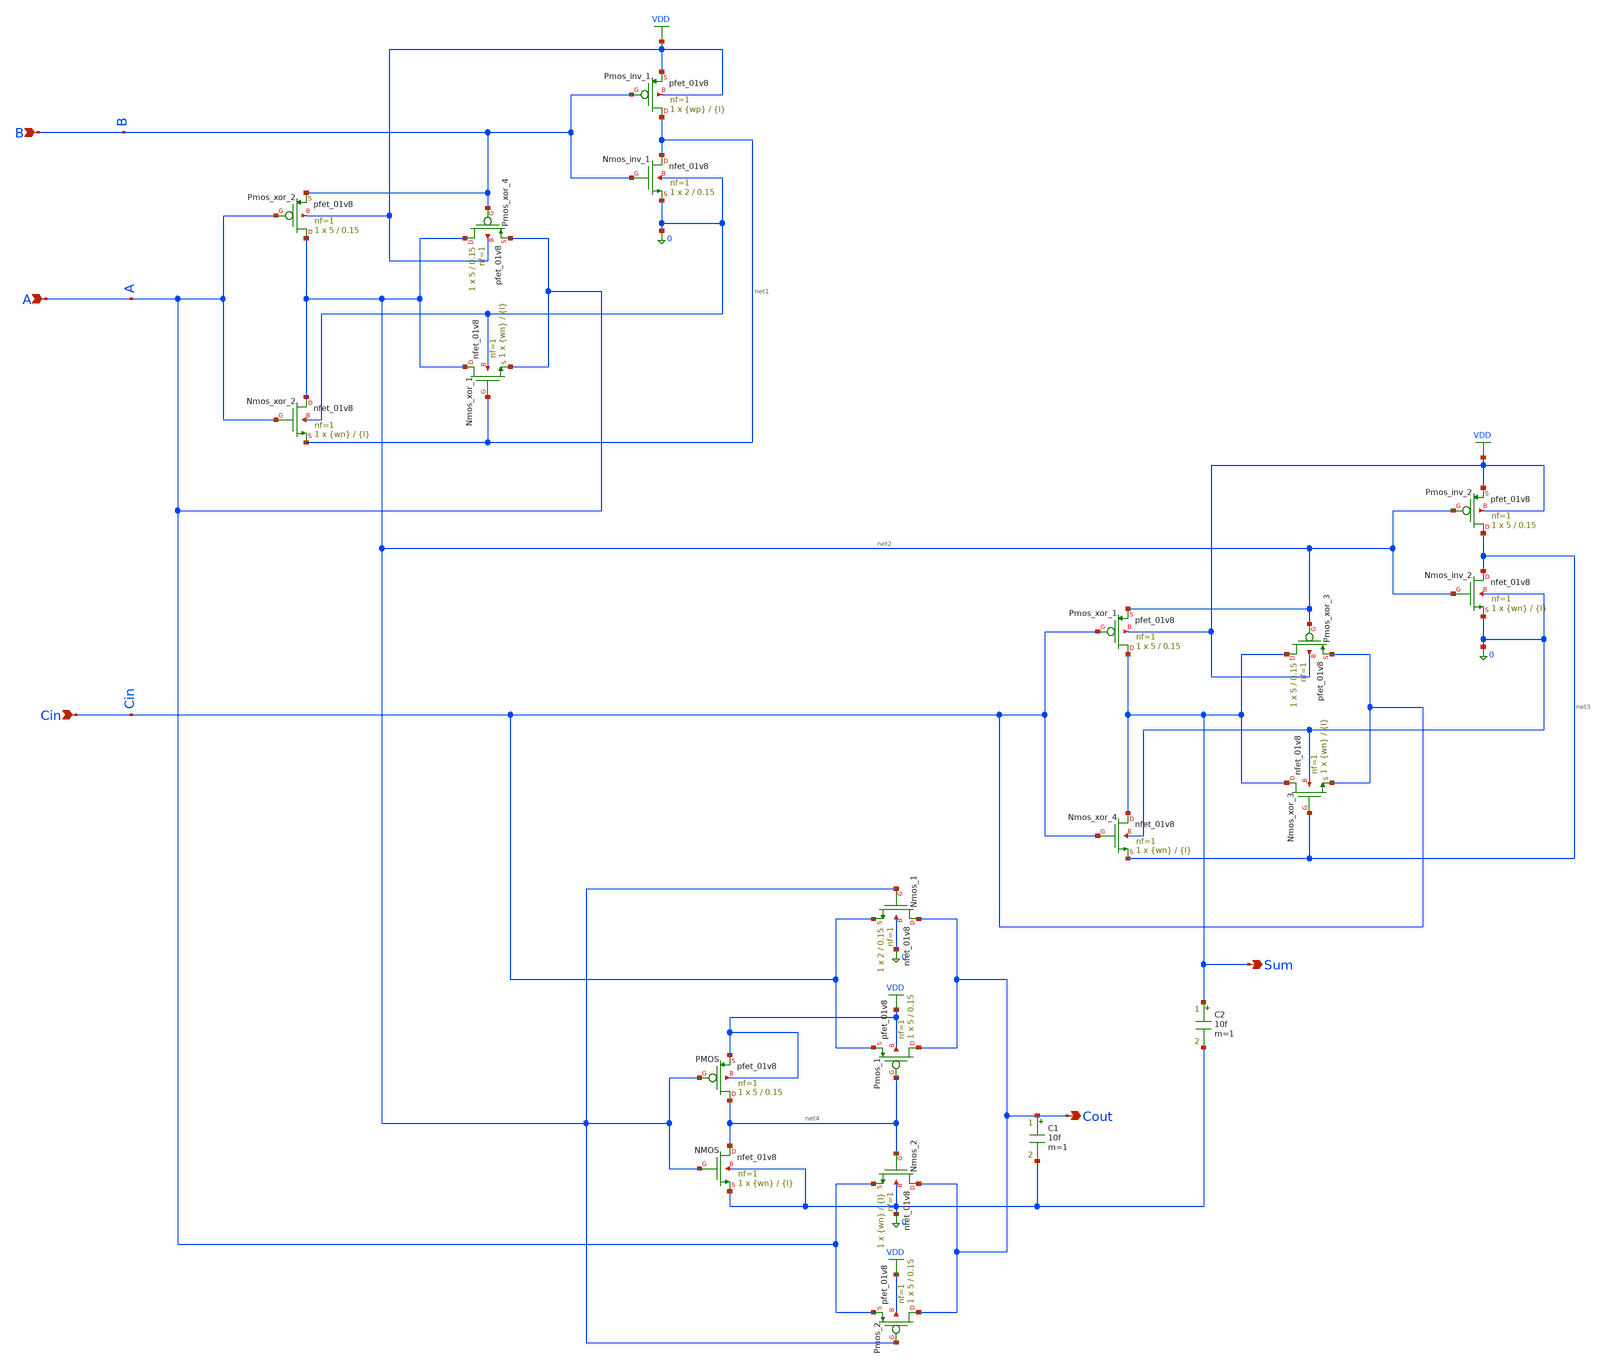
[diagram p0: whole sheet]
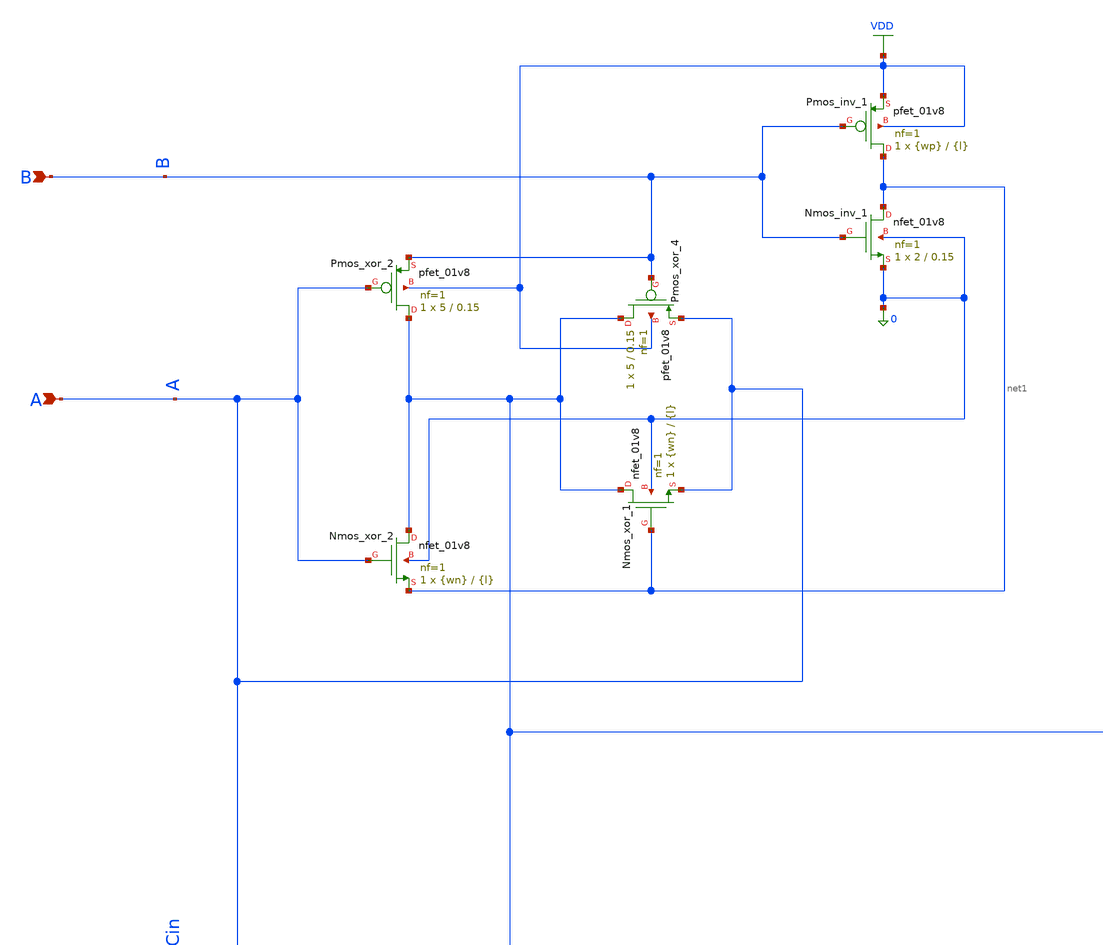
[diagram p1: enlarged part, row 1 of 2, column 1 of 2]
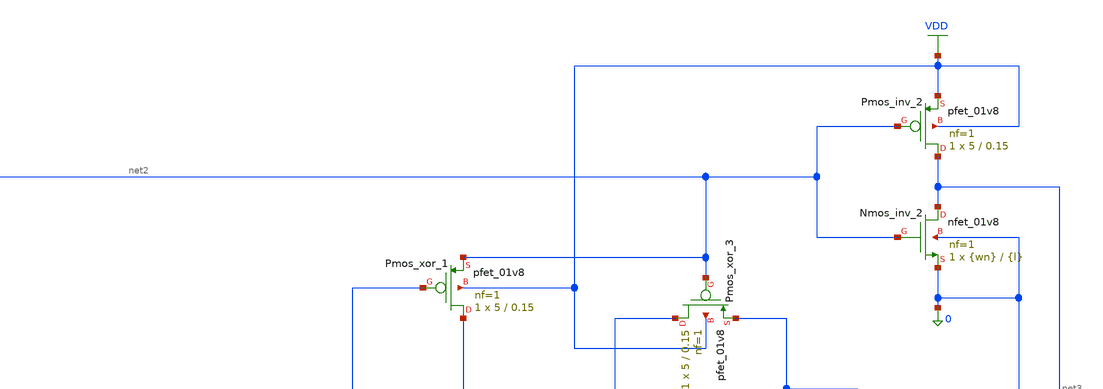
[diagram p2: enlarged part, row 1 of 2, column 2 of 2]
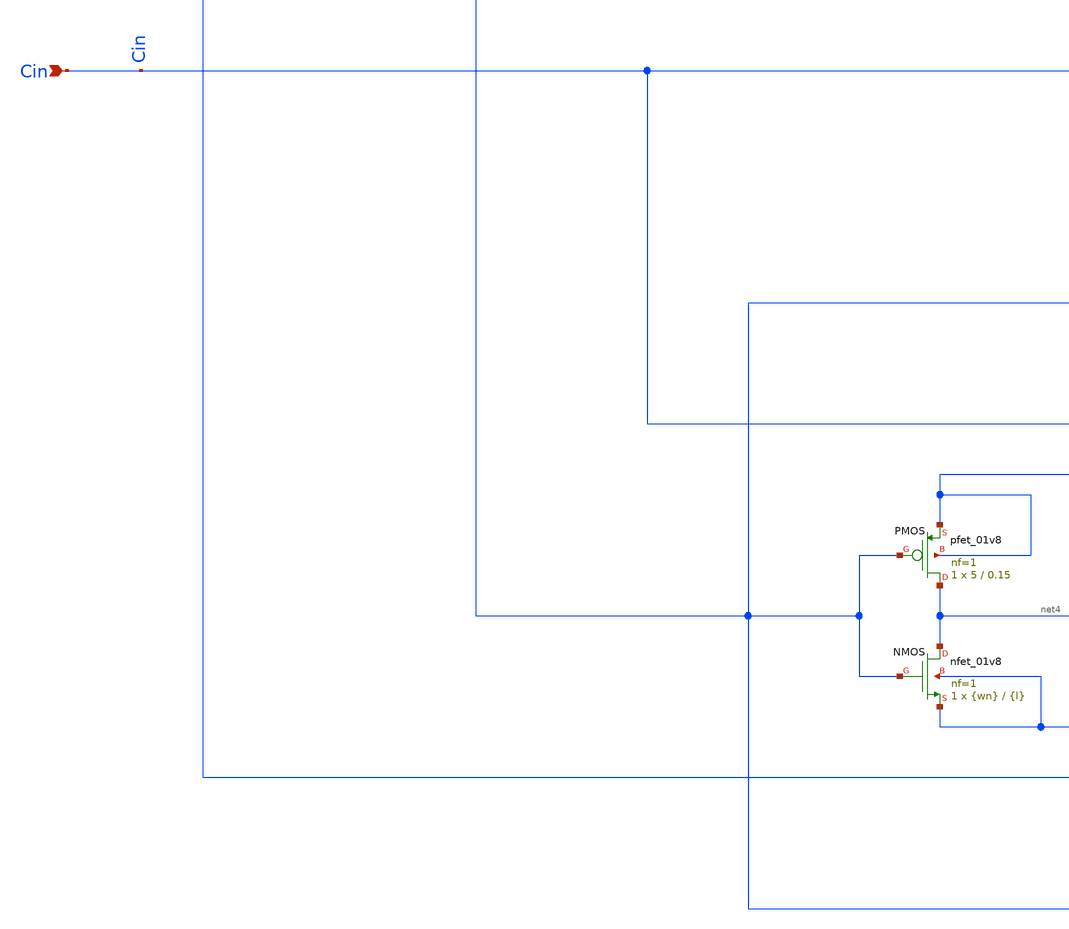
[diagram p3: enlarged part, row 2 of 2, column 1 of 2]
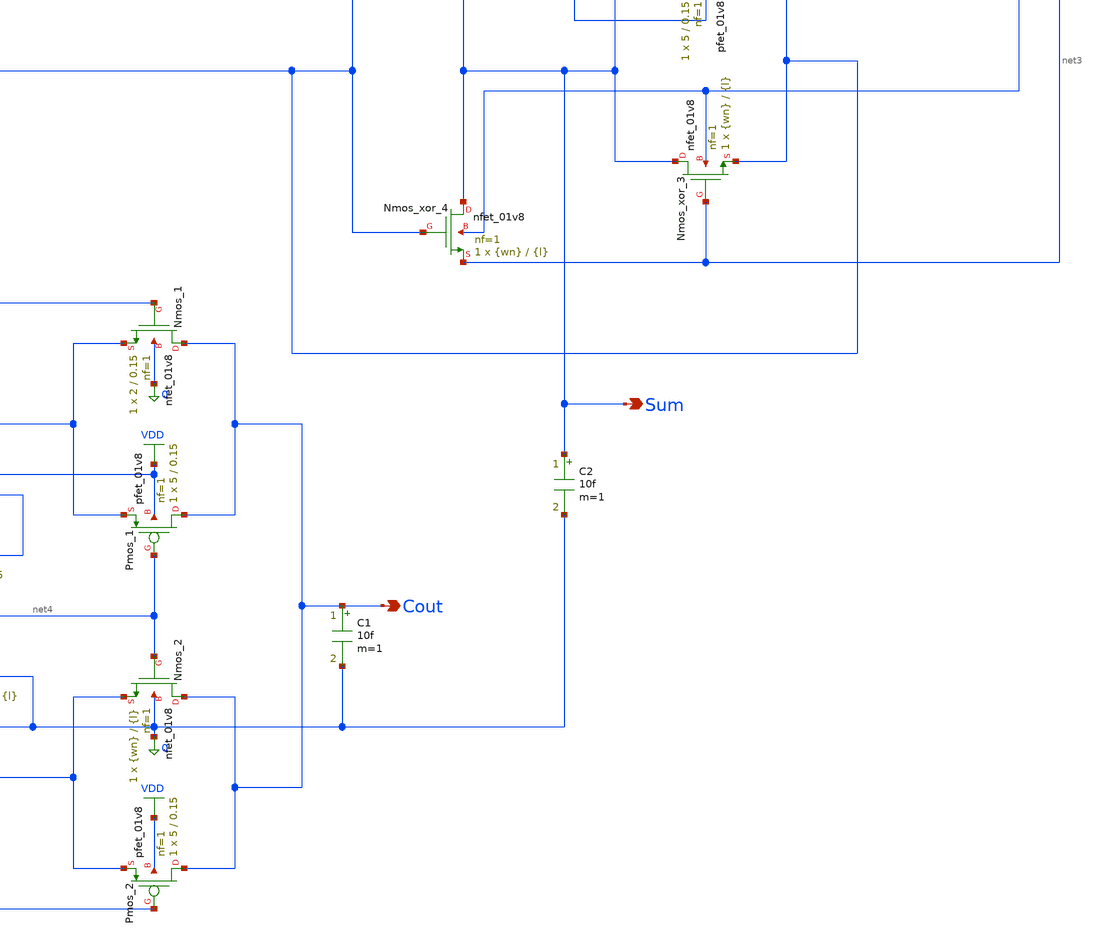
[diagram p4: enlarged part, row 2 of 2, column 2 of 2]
** sch_path: cells/full_adder_tg/xschem/FA_TG_1bit.sch
**.subckt FA_TG_1bit Sum Cout B A Cin
*.opin Sum
*.opin Cout
*.ipin B
*.ipin A
*.ipin Cin
XPmos_inv_1 net1 B VDD VDD sky130_fd_pr__pfet_01v8 L={l} W={wp} nf=1 ad='int((1 + 1)/2) * {wp} / 1 * 0.29'
+ as='int((1 + 2)/2) * {wp} / 1 * 0.29' pd='2*int((1 + 1)/2) * ({wp} / 1 + 0.29)' ps='2*int((1 + 2)/2) * ({wp} / 1 + 0.29)'
+ nrd='0.29 / {wp} ' nrs='0.29 / {wp} ' sa=0 sb=0 sd=0 mult=1 m=1
XNmos_inv_1 net1 B 0 0 sky130_fd_pr__nfet_01v8 L=0.15 W=2 nf=1 ad='int((1 + 1)/2) * 2 / 1 * 0.29' as='int((1 + 2)/2) * 2 / 1 * 0.29'
+ pd='2*int((1 + 1)/2) * (2 / 1 + 0.29)' ps='2*int((1 + 2)/2) * (2 / 1 + 0.29)' nrd='0.29 / 2 ' nrs='0.29 / 2 '
+ sa=0 sb=0 sd=0 mult=1 m=1
XPmos_xor_4 net2 B A VDD sky130_fd_pr__pfet_01v8 L=0.15 W=5 nf=1 ad='int((1 + 1)/2) * 5 / 1 * 0.29' as='int((1 + 2)/2) * 5 / 1 * 0.29'
+ pd='2*int((1 + 1)/2) * (5 / 1 + 0.29)' ps='2*int((1 + 2)/2) * (5 / 1 + 0.29)' nrd='0.29 / 5 ' nrs='0.29 / 5 '
+ sa=0 sb=0 sd=0 mult=1 m=1
XNmos_xor_1 net2 net1 A 0 sky130_fd_pr__nfet_01v8 L={l} W={wn} nf=1 ad='int((1 + 1)/2) * {wn} / 1 * 0.29'
+ as='int((1 + 2)/2) * {wn} / 1 * 0.29' pd='2*int((1 + 1)/2) * ({wn} / 1 + 0.29)' ps='2*int((1 + 2)/2) * ({wn} / 1 + 0.29)'
+ nrd='0.29 / {wn} ' nrs='0.29 / {wn} ' sa=0 sb=0 sd=0 mult=1 m=1
XPmos_xor_2 net2 A B VDD sky130_fd_pr__pfet_01v8 L=0.15 W=5 nf=1 ad='int((1 + 1)/2) * 5 / 1 * 0.29' as='int((1 + 2)/2) * 5 / 1 * 0.29'
+ pd='2*int((1 + 1)/2) * (5 / 1 + 0.29)' ps='2*int((1 + 2)/2) * (5 / 1 + 0.29)' nrd='0.29 / 5 ' nrs='0.29 / 5 '
+ sa=0 sb=0 sd=0 mult=1 m=1
XNmos_xor_2 net2 A net1 0 sky130_fd_pr__nfet_01v8 L={l} W={wn} nf=1 ad='int((1 + 1)/2) * {wn} / 1 * 0.29'
+ as='int((1 + 2)/2) * {wn} / 1 * 0.29' pd='2*int((1 + 1)/2) * ({wn} / 1 + 0.29)' ps='2*int((1 + 2)/2) * ({wn} / 1 + 0.29)'
+ nrd='0.29 / {wn} ' nrs='0.29 / {wn} ' sa=0 sb=0 sd=0 mult=1 m=1
XPmos_inv_2 net3 net2 VDD VDD sky130_fd_pr__pfet_01v8 L=0.15 W=5 nf=1 ad='int((1 + 1)/2) * 5 / 1 * 0.29'
+ as='int((1 + 2)/2) * 5 / 1 * 0.29' pd='2*int((1 + 1)/2) * (5 / 1 + 0.29)' ps='2*int((1 + 2)/2) * (5 / 1 + 0.29)'
+ nrd='0.29 / 5 ' nrs='0.29 / 5 ' sa=0 sb=0 sd=0 mult=1 m=1
XNmos_inv_2 net3 net2 0 0 sky130_fd_pr__nfet_01v8 L={l} W={wn} nf=1 ad='int((1 + 1)/2) * {wn} / 1 * 0.29'
+ as='int((1 + 2)/2) * {wn} / 1 * 0.29' pd='2*int((1 + 1)/2) * ({wn} / 1 + 0.29)' ps='2*int((1 + 2)/2) * ({wn} / 1 + 0.29)'
+ nrd='0.29 / {wn} ' nrs='0.29 / {wn} ' sa=0 sb=0 sd=0 mult=1 m=1
XPmos_xor_3 Sum net2 Cin VDD sky130_fd_pr__pfet_01v8 L=0.15 W=5 nf=1 ad='int((1 + 1)/2) * 5 / 1 * 0.29'
+ as='int((1 + 2)/2) * 5 / 1 * 0.29' pd='2*int((1 + 1)/2) * (5 / 1 + 0.29)' ps='2*int((1 + 2)/2) * (5 / 1 + 0.29)'
+ nrd='0.29 / 5 ' nrs='0.29 / 5 ' sa=0 sb=0 sd=0 mult=1 m=1
XNmos_xor_3 Sum net3 Cin 0 sky130_fd_pr__nfet_01v8 L={l} W={wn} nf=1 ad='int((1 + 1)/2) * {wn} / 1 * 0.29'
+ as='int((1 + 2)/2) * {wn} / 1 * 0.29' pd='2*int((1 + 1)/2) * ({wn} / 1 + 0.29)' ps='2*int((1 + 2)/2) * ({wn} / 1 + 0.29)'
+ nrd='0.29 / {wn} ' nrs='0.29 / {wn} ' sa=0 sb=0 sd=0 mult=1 m=1
XPmos_xor_1 Sum Cin net2 VDD sky130_fd_pr__pfet_01v8 L=0.15 W=5 nf=1 ad='int((1 + 1)/2) * 5 / 1 * 0.29'
+ as='int((1 + 2)/2) * 5 / 1 * 0.29' pd='2*int((1 + 1)/2) * (5 / 1 + 0.29)' ps='2*int((1 + 2)/2) * (5 / 1 + 0.29)'
+ nrd='0.29 / 5 ' nrs='0.29 / 5 ' sa=0 sb=0 sd=0 mult=1 m=1
XNmos_xor_4 Sum Cin net3 0 sky130_fd_pr__nfet_01v8 L={l} W={wn} nf=1 ad='int((1 + 1)/2) * {wn} / 1 * 0.29'
+ as='int((1 + 2)/2) * {wn} / 1 * 0.29' pd='2*int((1 + 1)/2) * ({wn} / 1 + 0.29)' ps='2*int((1 + 2)/2) * ({wn} / 1 + 0.29)'
+ nrd='0.29 / {wn} ' nrs='0.29 / {wn} ' sa=0 sb=0 sd=0 mult=1 m=1
C2 Sum 0 10f m=1
XNmos_1 Cout net2 Cin 0 sky130_fd_pr__nfet_01v8 L=0.15 W=2 nf=1 ad='int((1 + 1)/2) * 2 / 1 * 0.29' as='int((1 + 2)/2) * 2 / 1 * 0.29'
+ pd='2*int((1 + 1)/2) * (2 / 1 + 0.29)' ps='2*int((1 + 2)/2) * (2 / 1 + 0.29)' nrd='0.29 / 2 ' nrs='0.29 / 2 '
+ sa=0 sb=0 sd=0 mult=1 m=1
XPmos_1 Cout net4 Cin VDD sky130_fd_pr__pfet_01v8 L=0.15 W=5 nf=1 ad='int((1 + 1)/2) * 5 / 1 * 0.29'
+ as='int((1 + 2)/2) * 5 / 1 * 0.29' pd='2*int((1 + 1)/2) * (5 / 1 + 0.29)' ps='2*int((1 + 2)/2) * (5 / 1 + 0.29)'
+ nrd='0.29 / 5 ' nrs='0.29 / 5 ' sa=0 sb=0 sd=0 mult=1 m=1
XNmos_2 Cout net4 A 0 sky130_fd_pr__nfet_01v8 L={l} W={wn} nf=1 ad='int((1 + 1)/2) * {wn} / 1 * 0.29'
+ as='int((1 + 2)/2) * {wn} / 1 * 0.29' pd='2*int((1 + 1)/2) * ({wn} / 1 + 0.29)' ps='2*int((1 + 2)/2) * ({wn} / 1 + 0.29)'
+ nrd='0.29 / {wn} ' nrs='0.29 / {wn} ' sa=0 sb=0 sd=0 mult=1 m=1
XPmos_2 Cout net2 A VDD sky130_fd_pr__pfet_01v8 L=0.15 W=5 nf=1 ad='int((1 + 1)/2) * 5 / 1 * 0.29' as='int((1 + 2)/2) * 5 / 1 * 0.29'
+ pd='2*int((1 + 1)/2) * (5 / 1 + 0.29)' ps='2*int((1 + 2)/2) * (5 / 1 + 0.29)' nrd='0.29 / 5 ' nrs='0.29 / 5 '
+ sa=0 sb=0 sd=0 mult=1 m=1
XNMOS net4 net2 0 0 sky130_fd_pr__nfet_01v8 L={l} W={wn} nf=1 ad='int((1 + 1)/2) * {wn} / 1 * 0.29' as='int((1 + 2)/2) * {wn} / 1 * 0.29'
+ pd='2*int((1 + 1)/2) * ({wn} / 1 + 0.29)' ps='2*int((1 + 2)/2) * ({wn} / 1 + 0.29)' nrd='0.29 / {wn} '
+ nrs='0.29 / {wn} ' sa=0 sb=0 sd=0 mult=1 m=1
XPMOS net4 net2 VDD VDD sky130_fd_pr__pfet_01v8 L=0.15 W=5 nf=1 ad='int((1 + 1)/2) * 5 / 1 * 0.29' as='int((1 + 2)/2) * 5 / 1 * 0.29'
+ pd='2*int((1 + 1)/2) * (5 / 1 + 0.29)' ps='2*int((1 + 2)/2) * (5 / 1 + 0.29)' nrd='0.29 / 5 ' nrs='0.29 / 5 '
+ sa=0 sb=0 sd=0 mult=1 m=1
C1 Cout 0 10f m=1
**.ends
.GLOBAL VDD
.end
